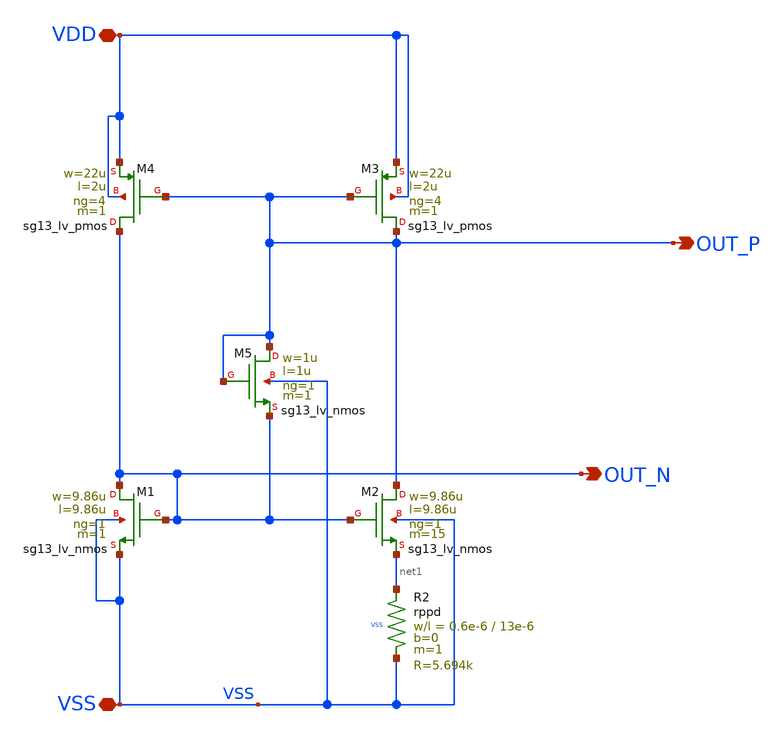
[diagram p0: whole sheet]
** sch_path: OTA_Telescopic/OTA_Telescopic_currentRef.sch
**.subckt OTA_Telescopic_currentRef VDD VSS OUT_P OUT_N
*.iopin VDD
*.iopin VSS
*.opin OUT_P
*.opin OUT_N
XM3 OUT_P OUT_P VDD VDD sg13_lv_pmos w=22u l=2u ng=4 m=1 mm_ok=1
XM2 OUT_P OUT_N net1 VSS sg13_lv_nmos w=9.86u l=9.86u ng=1 m=15 mm_ok=1
XM4 OUT_N OUT_P VDD VDD sg13_lv_pmos w=22u l=2u ng=4 m=1 mm_ok=1
XM1 OUT_N OUT_N VSS VSS sg13_lv_nmos w=9.86u l=9.86u ng=1 m=1 mm_ok=1
XM5 OUT_P OUT_P OUT_N VSS sg13_lv_nmos w=1u l=1u ng=1 m=1 mm_ok=1
XR2 net1 VSS VSS rppd w=0.6e-6 l=13e-6 m=1 b=0 mm_ok=1
**.ends
.end
